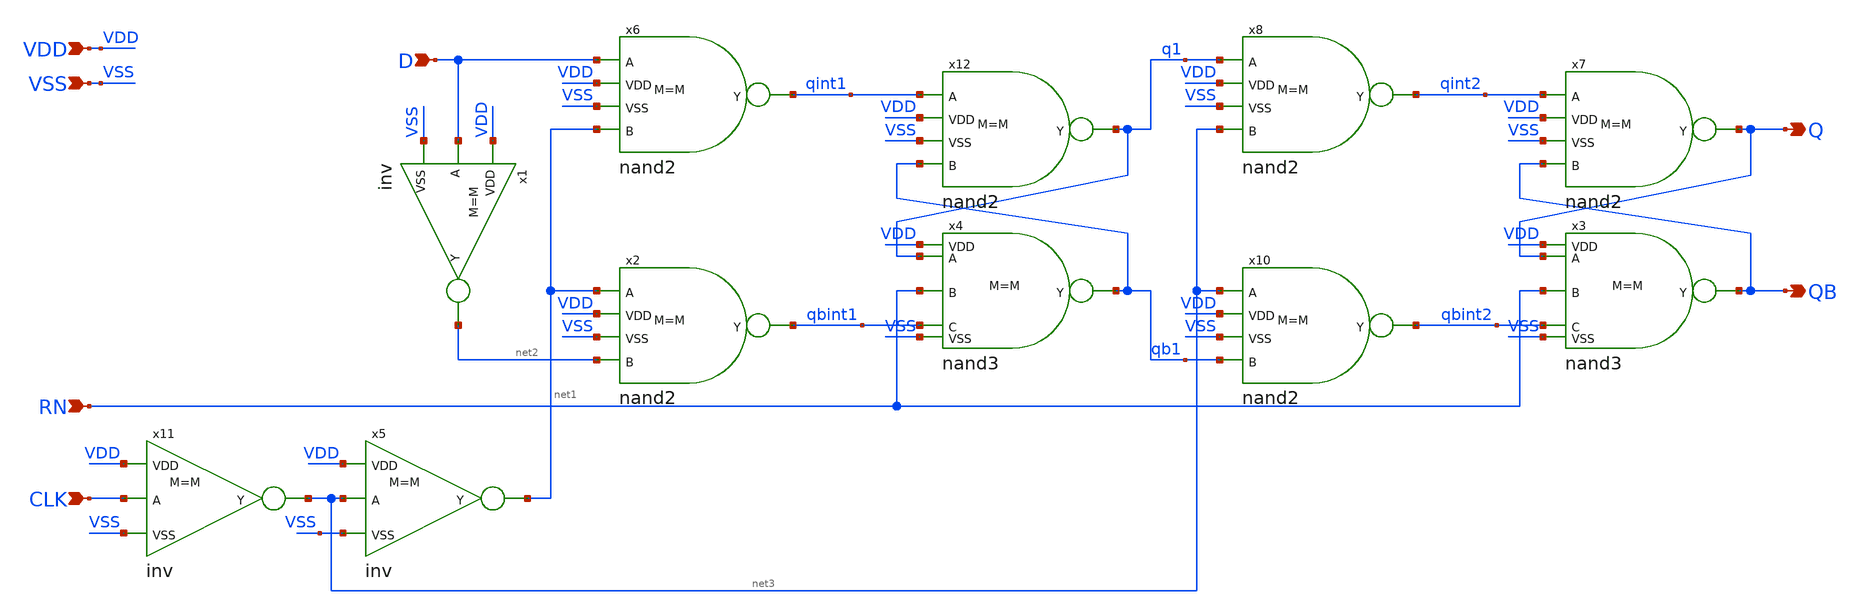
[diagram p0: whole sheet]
** sch_path: designs/dffr.sch
**.subckt dffr D CLK Q QB RN VDD VSS
*.ipin D
*.ipin CLK
*.opin Q
*.opin QB
*.ipin RN
*.ipin VDD
*.ipin VSS
x6 D qint1 net1 VDD VSS nand2 M=M
x2 net1 qbint1 net2 VDD VSS nand2 M=M
x5 net3 net1 VDD VSS inv M=M
x1 D net2 VDD VSS inv M=M
x7 qint2 Q QB VDD VSS nand2 M=M
x8 q1 qint2 net3 VDD VSS nand2 M=M
x10 net3 qbint2 qb1 VDD VSS nand2 M=M
x11 CLK net3 VDD VSS inv M=M
x3 Q RN qbint2 QB VDD VSS nand3 M=M
x12 qint1 q1 qb1 VDD VSS nand2 M=M
x4 q1 RN qbint1 qb1 VDD VSS nand3 M=M
**.ends
.end
